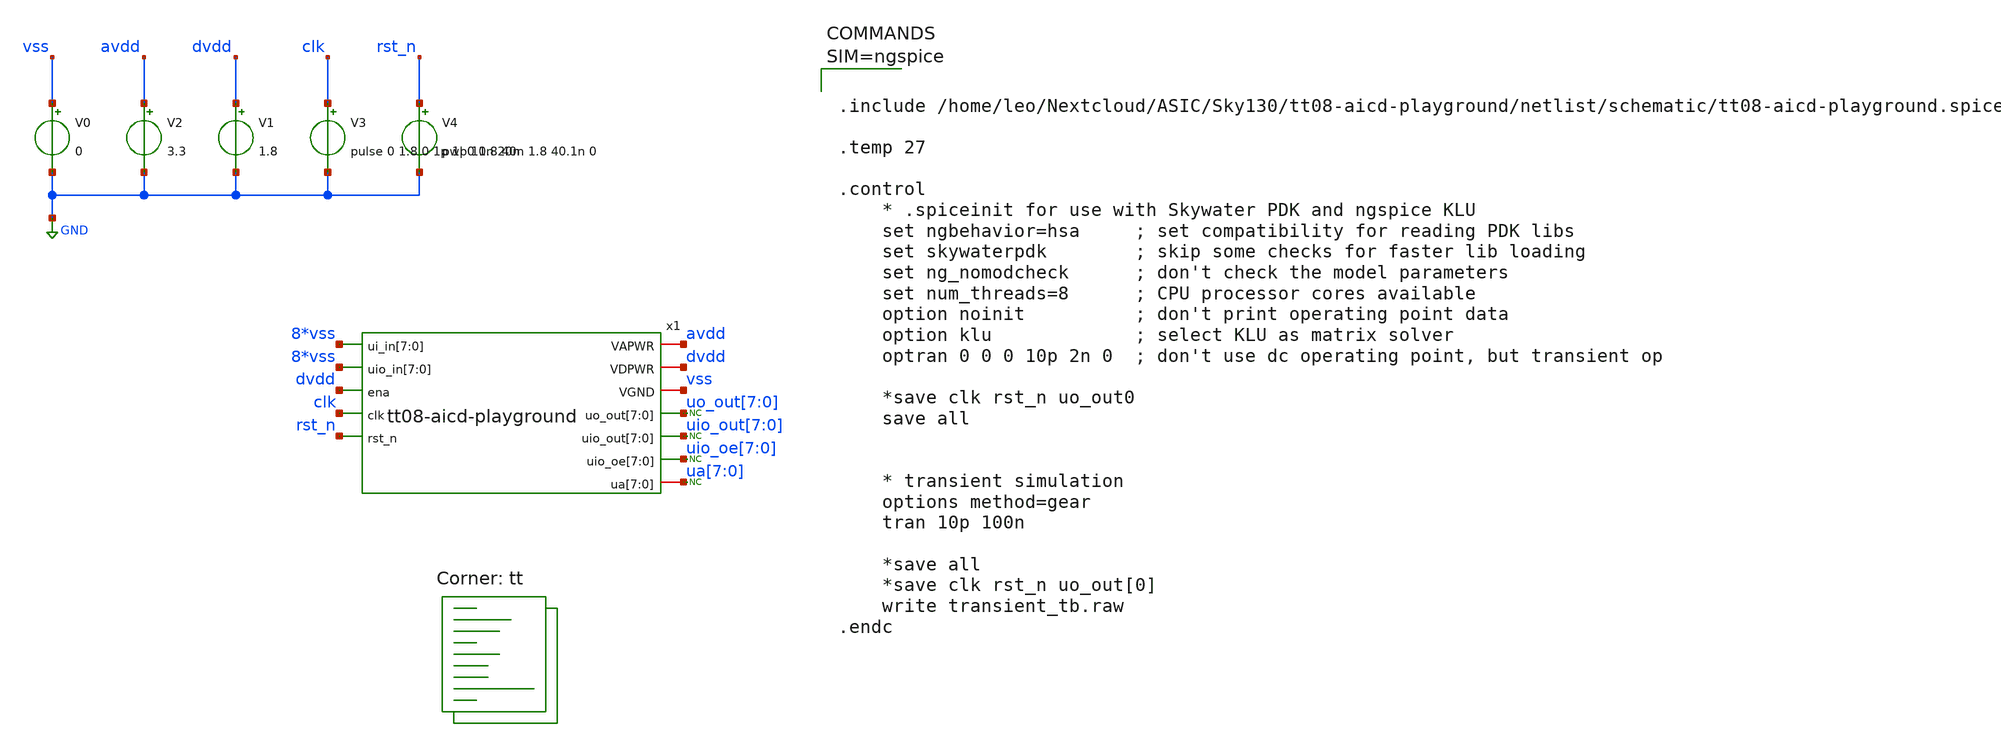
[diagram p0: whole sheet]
** sch_path: xschem/transient_tb.sch
**.subckt transient_tb
x1 avdd vss vss vss vss vss vss vss vss dvdd vss vss vss vss vss vss vss vss vss dvdd uo_out[7]
+ uo_out[6] uo_out[5] uo_out[4] uo_out[3] uo_out[2] uo_out[1] uo_out[0] clk rst_n uio_out[7] uio_out[6]
+ uio_out[5] uio_out[4] uio_out[3] uio_out[2] uio_out[1] uio_out[0] uio_oe[7] uio_oe[6] uio_oe[5] uio_oe[4]
+ uio_oe[3] uio_oe[2] uio_oe[1] uio_oe[0] ua[7] ua[6] ua[5] ua[4] ua[3] ua[2] ua[1] ua[0] tt08-aicd-playground
V0 vss GND 0
V2 avdd GND 3.3
V1 dvdd GND 1.8
V3 clk GND pulse 0 1.8 0 1p 1p 10n 20n
V4 rst_n GND pwl 0 1.8 40n 1.8 40.1n 0
* noconn uo_out[7:0]
* noconn uio_out[7:0]
* noconn uio_oe[7:0]
* noconn ua[7:0]
**** begin user architecture code
.lib $::SKYWATER_MODELS/sky130.lib.spice tt



.include /home/leo/Nextcloud/ASIC/Sky130/tt08-aicd-playground/netlist/schematic/tt08-aicd-playground.spice

.temp 27

.control
    * .spiceinit for use with Skywater PDK and ngspice KLU
    set ngbehavior=hsa     ; set compatibility for reading PDK libs
    set skywaterpdk        ; skip some checks for faster lib loading
    set ng_nomodcheck      ; don't check the model parameters
    set num_threads=8      ; CPU processor cores available
    option noinit          ; don't print operating point data
    option klu             ; select KLU as matrix solver
    optran 0 0 0 10p 2n 0  ; don't use dc operating point, but transient op

    *save clk rst_n uo_out0
    save all


    * transient simulation
    options method=gear
    tran 10p 100n

    *save all
    *save clk rst_n uo_out[0]
    write transient_tb.raw
.endc



**** end user architecture code
**.ends
.GLOBAL GND
.end
